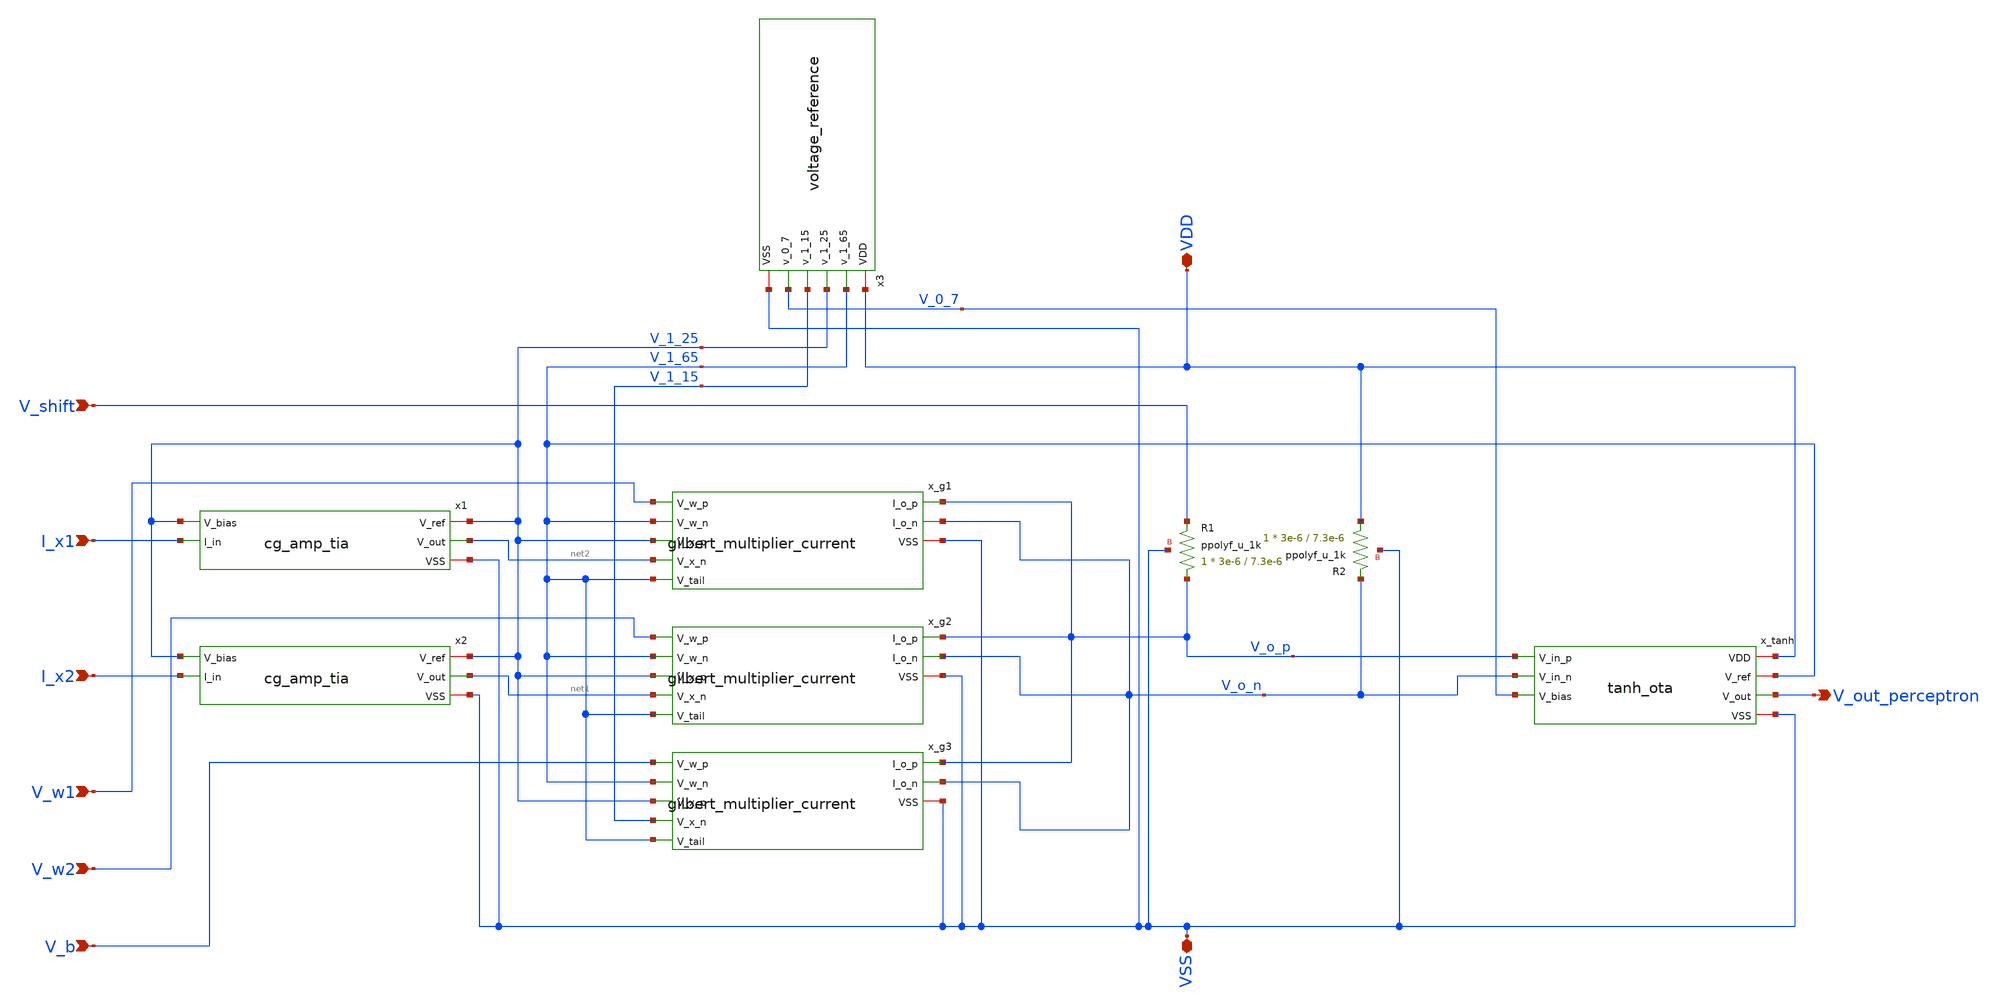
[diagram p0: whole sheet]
** sch_path: schematics/perceptron.sch
**.subckt perceptron VDD VSS I_x1 I_x2 V_w1 V_w2 V_b V_out_perceptron V_shift
*.iopin VDD
*.iopin VSS
*.ipin I_x1
*.ipin I_x2
*.ipin V_w1
*.ipin V_w2
*.ipin V_b
*.opin V_out_perceptron
*.ipin V_shift
x1 V_1_25 net2 V_1_25 I_x1 VSS cg_amp_tia
x2 V_1_25 net1 V_1_25 I_x2 VSS cg_amp_tia
x_g1 V_o_p V_o_n V_w1 V_1_65 V_1_25 net2 V_1_65 VSS gilbert_multiplier_current
x_g2 V_o_p V_o_n V_w2 V_1_65 V_1_25 net1 V_1_65 VSS gilbert_multiplier_current
x_g3 V_o_p V_o_n V_b V_1_65 V_1_25 V_1_15 V_1_65 VSS gilbert_multiplier_current
x_tanh VDD V_1_65 V_out_perceptron V_o_p V_o_n V_0_7 VSS tanh_ota
XR1 V_o_p V_shift VSS ppolyf_u_1k r_width=3e-6 r_length=7.3e-6 m=1
XR2 VDD V_o_n VSS ppolyf_u_1k r_width=3e-6 r_length=7.3e-6 m=1
x3 VDD V_1_65 V_1_25 V_1_15 V_0_7 VSS voltage_reference
**.ends

* expanding   symbol:  analog-perceptron-gf180mcu/schematics/cg_amp_tia.sym # of pins=5
** sym_path: schematics/cg_amp_tia.sym
** sch_path: schematics/cg_amp_tia.sch
.subckt cg_amp_tia V_ref V_out V_bias I_in VSS
*.iopin V_ref
*.iopin VSS
*.ipin I_in
*.ipin V_bias
*.opin V_out
XM1 V_out V_bias I_in VSS nfet_03v3 L=0.5u W=5u nf=1 ad='int((nf+1)/2) * W/nf * 0.18u' as='int((nf+2)/2) * W/nf * 0.18u'
+ pd='2*int((nf+1)/2) * (W/nf + 0.18u)' ps='2*int((nf+2)/2) * (W/nf + 0.18u)' nrd='0.18u / W' nrs='0.18u / W'
+ sa=0 sb=0 sd=0 m=1
XR1 V_out V_ref VSS ppolyf_u_1k r_width=3e-6 r_length=8.1e-6 m=1
.ends


* expanding   symbol:  analog-perceptron-gf180mcu/schematics/gilbert_multiplier_current.sym # of
*+ pins=8
** sym_path: schematics/gilbert_multiplier_current.sym
** sch_path: schematics/gilbert_multiplier_current.sch
.subckt gilbert_multiplier_current I_o_p I_o_n V_w_p V_w_n V_x_p V_x_n V_tail VSS
*.ipin V_x_p
*.ipin V_x_n
*.ipin V_tail
*.iopin VSS
*.ipin V_w_p
*.ipin V_w_n
*.opin I_o_n
*.opin I_o_p
XM1 net1 V_x_p net3 VSS nfet_03v3 L=0.5u W=10u nf=1 ad='int((nf+1)/2) * W/nf * 0.18u' as='int((nf+2)/2) * W/nf * 0.18u'
+ pd='2*int((nf+1)/2) * (W/nf + 0.18u)' ps='2*int((nf+2)/2) * (W/nf + 0.18u)' nrd='0.18u / W' nrs='0.18u / W'
+ sa=0 sb=0 sd=0 m=1
XM2 net2 V_x_n net4 VSS nfet_03v3 L=0.5u W=10u nf=1 ad='int((nf+1)/2) * W/nf * 0.18u' as='int((nf+2)/2) * W/nf * 0.18u'
+ pd='2*int((nf+1)/2) * (W/nf + 0.18u)' ps='2*int((nf+2)/2) * (W/nf + 0.18u)' nrd='0.18u / W' nrs='0.18u / W'
+ sa=0 sb=0 sd=0 m=1
XM3 I_o_n V_w_p net1 VSS nfet_03v3 L=0.5u W=10u nf=1 ad='int((nf+1)/2) * W/nf * 0.18u' as='int((nf+2)/2) * W/nf * 0.18u'
+ pd='2*int((nf+1)/2) * (W/nf + 0.18u)' ps='2*int((nf+2)/2) * (W/nf + 0.18u)' nrd='0.18u / W' nrs='0.18u / W'
+ sa=0 sb=0 sd=0 m=1
XM4 I_o_p V_w_n net1 VSS nfet_03v3 L=0.5u W=10u nf=1 ad='int((nf+1)/2) * W/nf * 0.18u' as='int((nf+2)/2) * W/nf * 0.18u'
+ pd='2*int((nf+1)/2) * (W/nf + 0.18u)' ps='2*int((nf+2)/2) * (W/nf + 0.18u)' nrd='0.18u / W' nrs='0.18u / W'
+ sa=0 sb=0 sd=0 m=1
XM5 I_o_n V_w_n net2 VSS nfet_03v3 L=0.5u W=10u nf=1 ad='int((nf+1)/2) * W/nf * 0.18u' as='int((nf+2)/2) * W/nf * 0.18u'
+ pd='2*int((nf+1)/2) * (W/nf + 0.18u)' ps='2*int((nf+2)/2) * (W/nf + 0.18u)' nrd='0.18u / W' nrs='0.18u / W'
+ sa=0 sb=0 sd=0 m=1
XM6 I_o_p V_w_p net2 VSS nfet_03v3 L=0.5u W=10u nf=1 ad='int((nf+1)/2) * W/nf * 0.18u' as='int((nf+2)/2) * W/nf * 0.18u'
+ pd='2*int((nf+1)/2) * (W/nf + 0.18u)' ps='2*int((nf+2)/2) * (W/nf + 0.18u)' nrd='0.18u / W' nrs='0.18u / W'
+ sa=0 sb=0 sd=0 m=1
XM7 net3 V_tail VSS VSS nfet_03v3 L=1u W=5u nf=1 ad='int((nf+1)/2) * W/nf * 0.18u' as='int((nf+2)/2) * W/nf * 0.18u'
+ pd='2*int((nf+1)/2) * (W/nf + 0.18u)' ps='2*int((nf+2)/2) * (W/nf + 0.18u)' nrd='0.18u / W' nrs='0.18u / W'
+ sa=0 sb=0 sd=0 m=1
XM8 net4 V_tail VSS VSS nfet_03v3 L=1u W=5u nf=1 ad='int((nf+1)/2) * W/nf * 0.18u' as='int((nf+2)/2) * W/nf * 0.18u'
+ pd='2*int((nf+1)/2) * (W/nf + 0.18u)' ps='2*int((nf+2)/2) * (W/nf + 0.18u)' nrd='0.18u / W' nrs='0.18u / W'
+ sa=0 sb=0 sd=0 m=1
XR1 net3 net4 VSS ppolyf_u_1k r_width=3e-6 r_length=46.2e-6 m=1
.ends


* expanding   symbol:  analog-perceptron-gf180mcu/schematics/tanh_ota.sym # of pins=7
** sym_path: schematics/tanh_ota.sym
** sch_path: schematics/tanh_ota.sch
.subckt tanh_ota VDD V_ref V_out V_in_p V_in_n V_bias VSS
*.iopin VDD
*.iopin VSS
*.ipin V_in_p
*.ipin V_in_n
*.ipin V_bias
*.opin V_out
*.iopin V_ref
XM1 net2 V_in_p net1 VSS nfet_03v3 L=0.5u W=10u nf=1 ad='int((nf+1)/2) * W/nf * 0.18u' as='int((nf+2)/2) * W/nf * 0.18u'
+ pd='2*int((nf+1)/2) * (W/nf + 0.18u)' ps='2*int((nf+2)/2) * (W/nf + 0.18u)' nrd='0.18u / W' nrs='0.18u / W'
+ sa=0 sb=0 sd=0 m=1
XM2 V_out V_in_n net1 VSS nfet_03v3 L=0.5u W=10u nf=1 ad='int((nf+1)/2) * W/nf * 0.18u' as='int((nf+2)/2) * W/nf * 0.18u'
+ pd='2*int((nf+1)/2) * (W/nf + 0.18u)' ps='2*int((nf+2)/2) * (W/nf + 0.18u)' nrd='0.18u / W' nrs='0.18u / W'
+ sa=0 sb=0 sd=0 m=1
XM3 net1 V_bias VSS VSS nfet_03v3 L=0.5u W=10u nf=1 ad='int((nf+1)/2) * W/nf * 0.18u' as='int((nf+2)/2) * W/nf * 0.18u'
+ pd='2*int((nf+1)/2) * (W/nf + 0.18u)' ps='2*int((nf+2)/2) * (W/nf + 0.18u)' nrd='0.18u / W' nrs='0.18u / W'
+ sa=0 sb=0 sd=0 m=1
XM4 net2 net2 VDD VDD pfet_03v3 L=0.5u W=20u nf=1 ad='int((nf+1)/2) * W/nf * 0.18u' as='int((nf+2)/2) * W/nf * 0.18u'
+ pd='2*int((nf+1)/2) * (W/nf + 0.18u)' ps='2*int((nf+2)/2) * (W/nf + 0.18u)' nrd='0.18u / W' nrs='0.18u / W'
+ sa=0 sb=0 sd=0 m=1
XM5 V_out net2 VDD VDD pfet_03v3 L=0.5u W=20u nf=1 ad='int((nf+1)/2) * W/nf * 0.18u' as='int((nf+2)/2) * W/nf * 0.18u'
+ pd='2*int((nf+1)/2) * (W/nf + 0.18u)' ps='2*int((nf+2)/2) * (W/nf + 0.18u)' nrd='0.18u / W' nrs='0.18u / W'
+ sa=0 sb=0 sd=0 m=1
XR1 V_out V_ref VSS ppolyf_u_1k r_width=3e-6 r_length=74.4e-6 m=1
.ends


* expanding   symbol:  analog-perceptron-gf180mcu/schematics/voltage_reference.sym # of pins=6
** sym_path: schematics/voltage_reference.sym
** sch_path: schematics/voltage_reference.sch
.subckt voltage_reference VDD v_1_65 v_1_25 v_1_15 v_0_7 VSS
*.iopin VDD
*.iopin VSS
*.opin v_1_65
*.opin v_1_15
*.opin v_0_7
*.opin v_1_25
XR1 V_I_1_65 VDD VSS ppolyf_u_1k r_width=1.5e-6 r_length=11.98e-6 m=24
XR2 V_I_1_25 V_I_1_65 VSS ppolyf_u_1k r_width=1.5e-6 r_length=2.78e-6 m=24
XR3 V_I_1_15 V_I_1_25 VSS ppolyf_u_1k r_width=1.5e-6 r_length=0.57e-6 m=24
XR4 V_I_0_7 V_I_1_15 VSS ppolyf_u_1k r_width=1.5e-6 r_length=3.15e-6 m=24
XR5 VSS V_I_0_7 VSS ppolyf_u_1k r_width=1.5e-6 r_length=4.99e-6 m=24
XM11 net2 V_pbias VDD VDD pfet_03v3 L=1u W=20u nf=1 ad='int((nf+1)/2) * W/nf * 0.18u' as='int((nf+2)/2) * W/nf * 0.18u'
+ pd='2*int((nf+1)/2) * (W/nf + 0.18u)' ps='2*int((nf+2)/2) * (W/nf + 0.18u)' nrd='0.18u / W' nrs='0.18u / W'
+ sa=0 sb=0 sd=0 m=1
XM12 net1 V_I_1_15 net2 VDD pfet_03v3 L=1u W=20u nf=1 ad='int((nf+1)/2) * W/nf * 0.18u' as='int((nf+2)/2) * W/nf * 0.18u'
+ pd='2*int((nf+1)/2) * (W/nf + 0.18u)' ps='2*int((nf+2)/2) * (W/nf + 0.18u)' nrd='0.18u / W' nrs='0.18u / W'
+ sa=0 sb=0 sd=0 m=1
XM13 v_1_15 v_1_15 net2 VDD pfet_03v3 L=1u W=20u nf=1 ad='int((nf+1)/2) * W/nf * 0.18u' as='int((nf+2)/2) * W/nf * 0.18u'
+ pd='2*int((nf+1)/2) * (W/nf + 0.18u)' ps='2*int((nf+2)/2) * (W/nf + 0.18u)' nrd='0.18u / W' nrs='0.18u / W'
+ sa=0 sb=0 sd=0 m=1
XM14 net1 net1 VSS VSS nfet_03v3 L=1u W=10u nf=1 ad='int((nf+1)/2) * W/nf * 0.18u' as='int((nf+2)/2) * W/nf * 0.18u'
+ pd='2*int((nf+1)/2) * (W/nf + 0.18u)' ps='2*int((nf+2)/2) * (W/nf + 0.18u)' nrd='0.18u / W' nrs='0.18u / W'
+ sa=0 sb=0 sd=0 m=1
XM15 v_1_15 net1 VSS VSS nfet_03v3 L=1u W=10u nf=1 ad='int((nf+1)/2) * W/nf * 0.18u' as='int((nf+2)/2) * W/nf * 0.18u'
+ pd='2*int((nf+1)/2) * (W/nf + 0.18u)' ps='2*int((nf+2)/2) * (W/nf + 0.18u)' nrd='0.18u / W' nrs='0.18u / W'
+ sa=0 sb=0 sd=0 m=1
XM16 net4 V_pbias VDD VDD pfet_03v3 L=1u W=20u nf=1 ad='int((nf+1)/2) * W/nf * 0.18u' as='int((nf+2)/2) * W/nf * 0.18u'
+ pd='2*int((nf+1)/2) * (W/nf + 0.18u)' ps='2*int((nf+2)/2) * (W/nf + 0.18u)' nrd='0.18u / W' nrs='0.18u / W'
+ sa=0 sb=0 sd=0 m=1
XM17 net3 V_I_0_7 net4 VDD pfet_03v3 L=1u W=20u nf=1 ad='int((nf+1)/2) * W/nf * 0.18u' as='int((nf+2)/2) * W/nf * 0.18u'
+ pd='2*int((nf+1)/2) * (W/nf + 0.18u)' ps='2*int((nf+2)/2) * (W/nf + 0.18u)' nrd='0.18u / W' nrs='0.18u / W'
+ sa=0 sb=0 sd=0 m=1
XM18 v_0_7 v_0_7 net4 VDD pfet_03v3 L=1u W=20u nf=1 ad='int((nf+1)/2) * W/nf * 0.18u' as='int((nf+2)/2) * W/nf * 0.18u'
+ pd='2*int((nf+1)/2) * (W/nf + 0.18u)' ps='2*int((nf+2)/2) * (W/nf + 0.18u)' nrd='0.18u / W' nrs='0.18u / W'
+ sa=0 sb=0 sd=0 m=1
XM19 net3 net3 VSS VSS nfet_03v3 L=1u W=10u nf=1 ad='int((nf+1)/2) * W/nf * 0.18u' as='int((nf+2)/2) * W/nf * 0.18u'
+ pd='2*int((nf+1)/2) * (W/nf + 0.18u)' ps='2*int((nf+2)/2) * (W/nf + 0.18u)' nrd='0.18u / W' nrs='0.18u / W'
+ sa=0 sb=0 sd=0 m=1
XM20 v_0_7 net3 VSS VSS nfet_03v3 L=1u W=10u nf=1 ad='int((nf+1)/2) * W/nf * 0.18u' as='int((nf+2)/2) * W/nf * 0.18u'
+ pd='2*int((nf+1)/2) * (W/nf + 0.18u)' ps='2*int((nf+2)/2) * (W/nf + 0.18u)' nrd='0.18u / W' nrs='0.18u / W'
+ sa=0 sb=0 sd=0 m=1
XM21 VDD net10 v_1_25 VSS nfet_03v3 L=1u W=100u nf=1 ad='int((nf+1)/2) * W/nf * 0.18u' as='int((nf+2)/2) * W/nf * 0.18u'
+ pd='2*int((nf+1)/2) * (W/nf + 0.18u)' ps='2*int((nf+2)/2) * (W/nf + 0.18u)' nrd='0.18u / W' nrs='0.18u / W'
+ sa=0 sb=0 sd=0 m=1
XR6 VSS v_1_25 VSS ppolyf_u_1k r_width=3e-6 r_length=30e-6 m=1
XM22 V_pbias V_pbias VDD VDD pfet_03v3 L=1u W=10u nf=1 ad='int((nf+1)/2) * W/nf * 0.18u' as='int((nf+2)/2) * W/nf * 0.18u'
+ pd='2*int((nf+1)/2) * (W/nf + 0.18u)' ps='2*int((nf+2)/2) * (W/nf + 0.18u)' nrd='0.18u / W' nrs='0.18u / W'
+ sa=0 sb=0 sd=0 m=1
XR7 VSS V_pbias VSS ppolyf_u_1k r_width=3e-6 r_length=150e-6 m=1
XM1 net6 V_I_1_65 net5 VSS nfet_03v3 L=2u W=10u nf=1 ad='int((nf+1)/2) * W/nf * 0.18u' as='int((nf+2)/2) * W/nf * 0.18u'
+ pd='2*int((nf+1)/2) * (W/nf + 0.18u)' ps='2*int((nf+2)/2) * (W/nf + 0.18u)' nrd='0.18u / W' nrs='0.18u / W'
+ sa=0 sb=0 sd=0 m=1
XM2 net7 v_1_65 net5 VSS nfet_03v3 L=2u W=10u nf=1 ad='int((nf+1)/2) * W/nf * 0.18u' as='int((nf+2)/2) * W/nf * 0.18u'
+ pd='2*int((nf+1)/2) * (W/nf + 0.18u)' ps='2*int((nf+2)/2) * (W/nf + 0.18u)' nrd='0.18u / W' nrs='0.18u / W'
+ sa=0 sb=0 sd=0 m=1
XM3 net5 V_nbias VSS VSS nfet_03v3 L=2u W=10u nf=1 ad='int((nf+1)/2) * W/nf * 0.18u' as='int((nf+2)/2) * W/nf * 0.18u'
+ pd='2*int((nf+1)/2) * (W/nf + 0.18u)' ps='2*int((nf+2)/2) * (W/nf + 0.18u)' nrd='0.18u / W' nrs='0.18u / W'
+ sa=0 sb=0 sd=0 m=1
XM4 net6 net6 VDD VDD pfet_03v3 L=2u W=20u nf=1 ad='int((nf+1)/2) * W/nf * 0.18u' as='int((nf+2)/2) * W/nf * 0.18u'
+ pd='2*int((nf+1)/2) * (W/nf + 0.18u)' ps='2*int((nf+2)/2) * (W/nf + 0.18u)' nrd='0.18u / W' nrs='0.18u / W'
+ sa=0 sb=0 sd=0 m=1
XM5 net7 net6 VDD VDD pfet_03v3 L=2u W=20u nf=1 ad='int((nf+1)/2) * W/nf * 0.18u' as='int((nf+2)/2) * W/nf * 0.18u'
+ pd='2*int((nf+1)/2) * (W/nf + 0.18u)' ps='2*int((nf+2)/2) * (W/nf + 0.18u)' nrd='0.18u / W' nrs='0.18u / W'
+ sa=0 sb=0 sd=0 m=1
XM23 V_nbias V_nbias VSS VSS nfet_03v3 L=1u W=10u nf=1 ad='int((nf+1)/2) * W/nf * 0.18u' as='int((nf+2)/2) * W/nf * 0.18u'
+ pd='2*int((nf+1)/2) * (W/nf + 0.18u)' ps='2*int((nf+2)/2) * (W/nf + 0.18u)' nrd='0.18u / W' nrs='0.18u / W'
+ sa=0 sb=0 sd=0 m=1
XR8 V_nbias VDD VSS ppolyf_u_1k r_width=3e-6 r_length=150e-6 m=1
XM6 net9 V_I_1_25 net8 VSS nfet_03v3 L=2u W=10u nf=1 ad='int((nf+1)/2) * W/nf * 0.18u' as='int((nf+2)/2) * W/nf * 0.18u'
+ pd='2*int((nf+1)/2) * (W/nf + 0.18u)' ps='2*int((nf+2)/2) * (W/nf + 0.18u)' nrd='0.18u / W' nrs='0.18u / W'
+ sa=0 sb=0 sd=0 m=1
XM7 net10 v_1_25 net8 VSS nfet_03v3 L=2u W=10u nf=1 ad='int((nf+1)/2) * W/nf * 0.18u' as='int((nf+2)/2) * W/nf * 0.18u'
+ pd='2*int((nf+1)/2) * (W/nf + 0.18u)' ps='2*int((nf+2)/2) * (W/nf + 0.18u)' nrd='0.18u / W' nrs='0.18u / W'
+ sa=0 sb=0 sd=0 m=1
XM8 net8 V_nbias VSS VSS nfet_03v3 L=2u W=10u nf=1 ad='int((nf+1)/2) * W/nf * 0.18u' as='int((nf+2)/2) * W/nf * 0.18u'
+ pd='2*int((nf+1)/2) * (W/nf + 0.18u)' ps='2*int((nf+2)/2) * (W/nf + 0.18u)' nrd='0.18u / W' nrs='0.18u / W'
+ sa=0 sb=0 sd=0 m=1
XM9 net9 net9 VDD VDD pfet_03v3 L=2u W=20u nf=1 ad='int((nf+1)/2) * W/nf * 0.18u' as='int((nf+2)/2) * W/nf * 0.18u'
+ pd='2*int((nf+1)/2) * (W/nf + 0.18u)' ps='2*int((nf+2)/2) * (W/nf + 0.18u)' nrd='0.18u / W' nrs='0.18u / W'
+ sa=0 sb=0 sd=0 m=1
XM10 net10 net9 VDD VDD pfet_03v3 L=2u W=20u nf=1 ad='int((nf+1)/2) * W/nf * 0.18u' as='int((nf+2)/2) * W/nf * 0.18u'
+ pd='2*int((nf+1)/2) * (W/nf + 0.18u)' ps='2*int((nf+2)/2) * (W/nf + 0.18u)' nrd='0.18u / W' nrs='0.18u / W'
+ sa=0 sb=0 sd=0 m=1
XM24 VDD net7 v_1_65 VSS nfet_03v3 L=1u W=100u nf=1 ad='int((nf+1)/2) * W/nf * 0.18u' as='int((nf+2)/2) * W/nf * 0.18u'
+ pd='2*int((nf+1)/2) * (W/nf + 0.18u)' ps='2*int((nf+2)/2) * (W/nf + 0.18u)' nrd='0.18u / W' nrs='0.18u / W'
+ sa=0 sb=0 sd=0 m=1
XR9 VSS v_1_65 VSS ppolyf_u_1k r_width=3e-6 r_length=30e-6 m=1
.ends

.end
